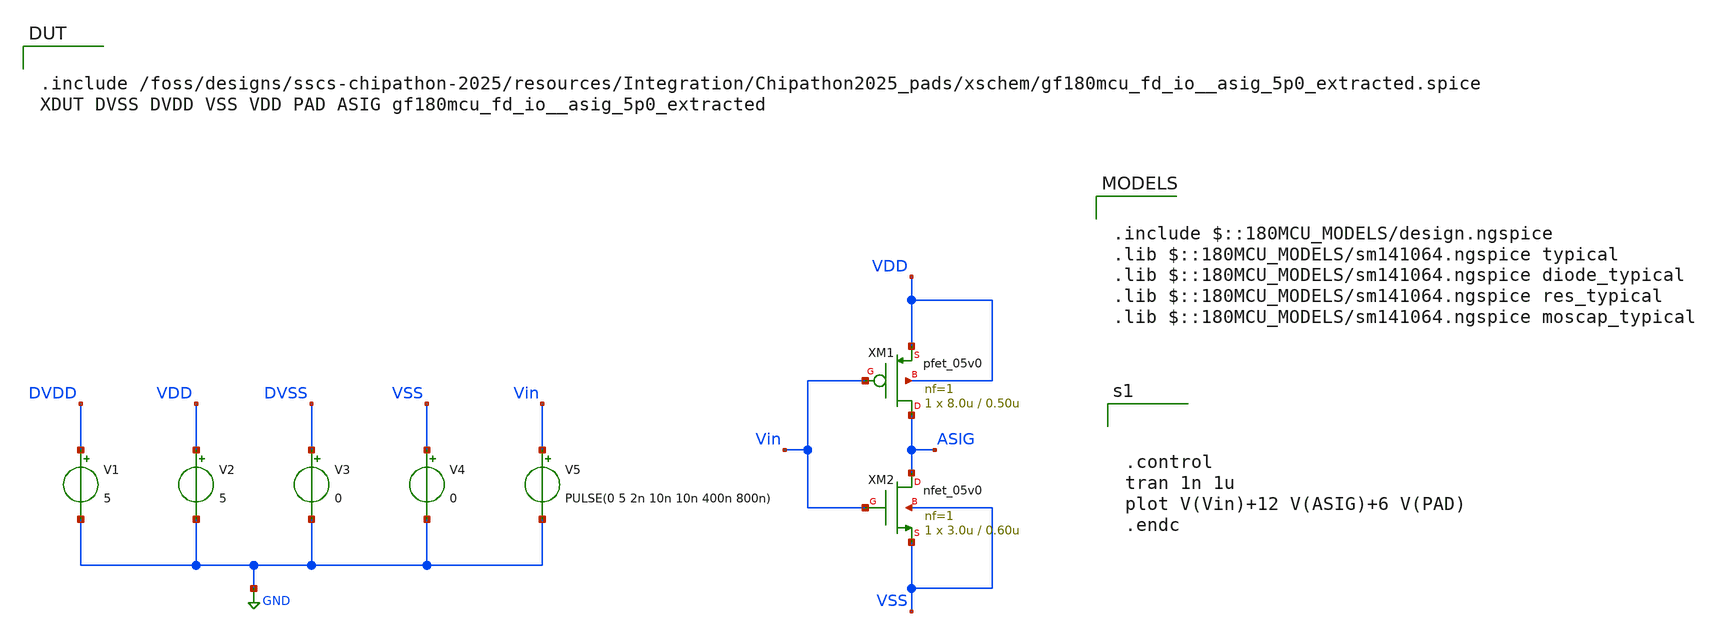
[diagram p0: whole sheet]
** sch_path: designs/Chipathon2025_pads/xschem/asig5V_tran_tb.sch
**.subckt asig5V_tran_tb
V1 DVDD GND 5
V2 VDD GND 5
V3 DVSS GND 0
V4 VSS GND 0
V5 Vin GND PULSE(0 5 2n 10n 10n 400n 800n)
XM1 ASIG Vin VDD VDD pfet_05v0 L=0.50u W=8.0u nf=1 ad='int((nf+1)/2) * W/nf * 0.18u' as='int((nf+2)/2) * W/nf * 0.18u'
+ pd='2*int((nf+1)/2) * (W/nf + 0.18u)' ps='2*int((nf+2)/2) * (W/nf + 0.18u)' nrd='0.18u / W' nrs='0.18u / W'
+ sa=0 sb=0 sd=0 m=1
XM2 ASIG Vin VSS VSS nfet_05v0 L=0.60u W=3.0u nf=1 ad='int((nf+1)/2) * W/nf * 0.18u' as='int((nf+2)/2) * W/nf * 0.18u'
+ pd='2*int((nf+1)/2) * (W/nf + 0.18u)' ps='2*int((nf+2)/2) * (W/nf + 0.18u)' nrd='0.18u / W' nrs='0.18u / W'
+ sa=0 sb=0 sd=0 m=1
**** begin user architecture code

.include /foss/designs/sscs-chipathon-2025/resources/Integration/Chipathon2025_pads/xschem/gf180mcu_fd_io__asig_5p0_extracted.spice
XDUT DVSS DVDD VSS VDD PAD ASIG gf180mcu_fd_io__asig_5p0_extracted


.include $::180MCU_MODELS/design.ngspice
.lib $::180MCU_MODELS/sm141064.ngspice typical
.lib $::180MCU_MODELS/sm141064.ngspice diode_typical
.lib $::180MCU_MODELS/sm141064.ngspice res_typical
.lib $::180MCU_MODELS/sm141064.ngspice moscap_typical




.control
tran 1n 1u
plot V(Vin)+12 V(ASIG)+6 V(PAD)
.endc


**** end user architecture code
**.ends
.GLOBAL GND
.end
